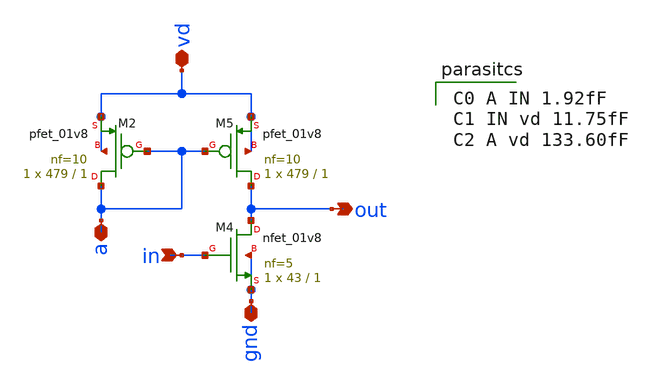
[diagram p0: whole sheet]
** sch_path: xschem/amp-cs.sch
**.subckt amp-cs in vd gnd a out
*.ipin in
*.iopin vd
*.iopin gnd
*.iopin a
*.opin out
XM4 out in gnd gnd sky130_fd_pr__nfet_01v8 L=1 W=43 nf=5 ad='int((nf+1)/2) * W/nf * 0.29' as='int((nf+2)/2) * W/nf * 0.29'
+ pd='2*int((nf+1)/2) * (W/nf + 0.29)' ps='2*int((nf+2)/2) * (W/nf + 0.29)' nrd='0.29 / W' nrs='0.29 / W'
+ sa=0 sb=0 sd=0 mult=1 m=1
XM5 out a vd vd sky130_fd_pr__pfet_01v8 L=1 W=479 nf=10 ad='int((nf+1)/2) * W/nf * 0.29' as='int((nf+2)/2) * W/nf * 0.29'
+ pd='2*int((nf+1)/2) * (W/nf + 0.29)' ps='2*int((nf+2)/2) * (W/nf + 0.29)' nrd='0.29 / W' nrs='0.29 / W'
+ sa=0 sb=0 sd=0 mult=1 m=1
XM2 a a vd vd sky130_fd_pr__pfet_01v8 L=1 W=479 nf=10 ad='int((nf+1)/2) * W/nf * 0.29' as='int((nf+2)/2) * W/nf * 0.29'
+ pd='2*int((nf+1)/2) * (W/nf + 0.29)' ps='2*int((nf+2)/2) * (W/nf + 0.29)' nrd='0.29 / W' nrs='0.29 / W'
+ sa=0 sb=0 sd=0 mult=1 m=1
**** begin user architecture code

C0 A IN 1.92fF
C1 IN vd 11.75fF
C2 A vd 133.60fF

**** end user architecture code
**.ends
.end
